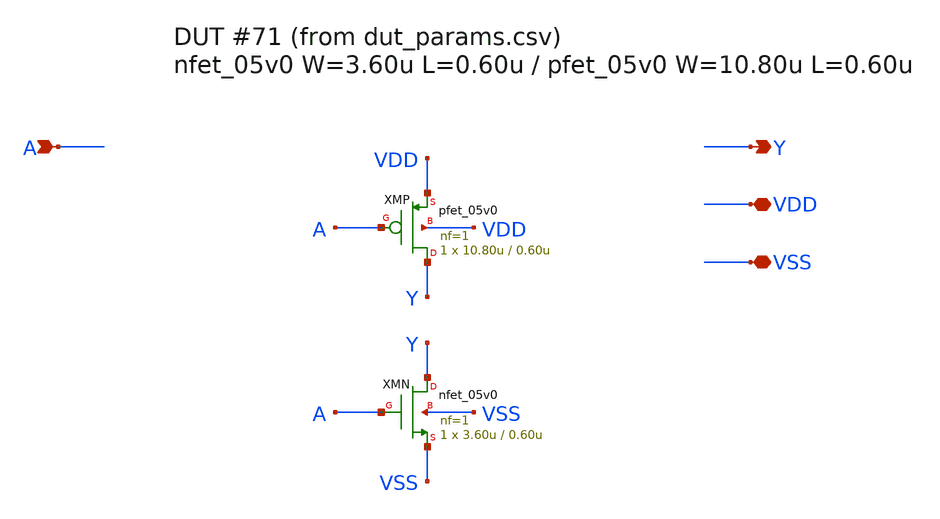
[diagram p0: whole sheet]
** sch_path: inverter_matrix/dut/inv_dut_071.sch
**.subckt inv_dut_071 A Y VDD VSS
*.ipin A
*.opin Y
*.iopin VDD
*.iopin VSS
XMP Y A VDD VDD pfet_05v0 L=0.60u W=10.80u nf=1 ad='int((nf+1)/2) * W/nf * 0.18u' as='int((nf+2)/2) * W/nf * 0.18u'
+ pd='2*int((nf+1)/2) * (W/nf + 0.18u)' ps='2*int((nf+2)/2) * (W/nf + 0.18u)' nrd='0.18u / W' nrs='0.18u / W'
+ sa=0 sb=0 sd=0 m=1
XMN Y A VSS VSS nfet_05v0 L=0.60u W=3.60u nf=1 ad='int((nf+1)/2) * W/nf * 0.18u' as='int((nf+2)/2) * W/nf * 0.18u'
+ pd='2*int((nf+1)/2) * (W/nf + 0.18u)' ps='2*int((nf+2)/2) * (W/nf + 0.18u)' nrd='0.18u / W' nrs='0.18u / W'
+ sa=0 sb=0 sd=0 m=1
**.ends
.end
